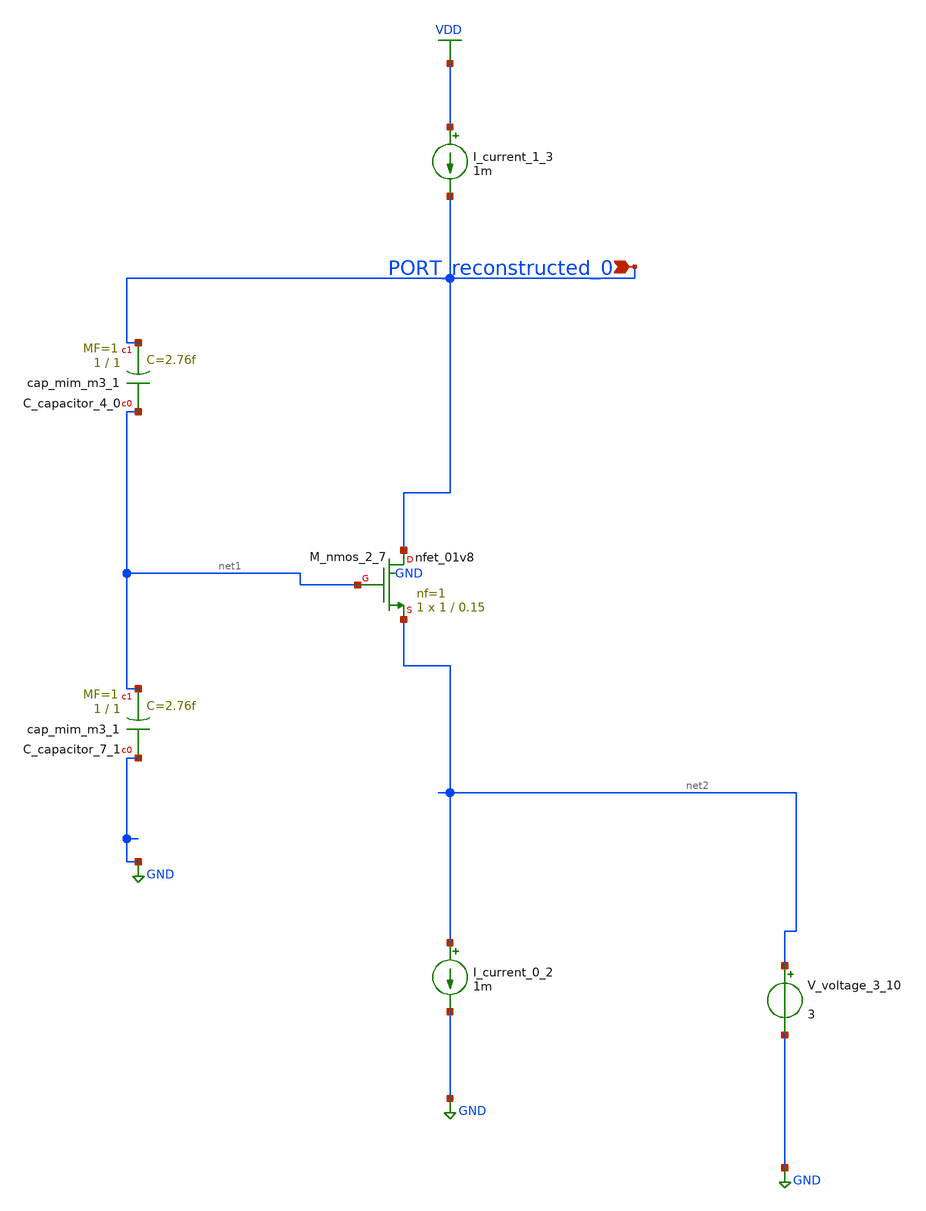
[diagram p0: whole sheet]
** sch_path: schematics/AMSNet/538.sch
**.subckt 538 PORT_reconstructed_0
*.ipin PORT_reconstructed_0
XC_capacitor_4_0 net1 PORT_reconstructed_0 sky130_fd_pr__cap_mim_m3_1 W=1 L=1 MF=1 m=1
XC_capacitor_7_1 GND net1 sky130_fd_pr__cap_mim_m3_1 W=1 L=1 MF=1 m=1
I_current_0_2 net2 GND 1m
I_current_1_3 VDD PORT_reconstructed_0 1m
XM_nmos_2_7 PORT_reconstructed_0 net1 net2 GND sky130_fd_pr__nfet_01v8 L=0.15 W=1 nf=1 ad='int((1 + 1)/2) * 1 / 1 * 0.29'
+ as='int((1 + 2)/2) * 1 / 1 * 0.29' pd='2*int((1 + 1)/2) * (1 / 1 + 0.29)' ps='2*int((1 + 2)/2) * (1 / 1 + 0.29)'
+ nrd='0.29 / 1 ' nrs='0.29 / 1 ' sa=0 sb=0 sd=0 mult=1 m=1
V_voltage_3_10 net2 GND 3
**.ends
.GLOBAL GND
.GLOBAL VDD
.end
